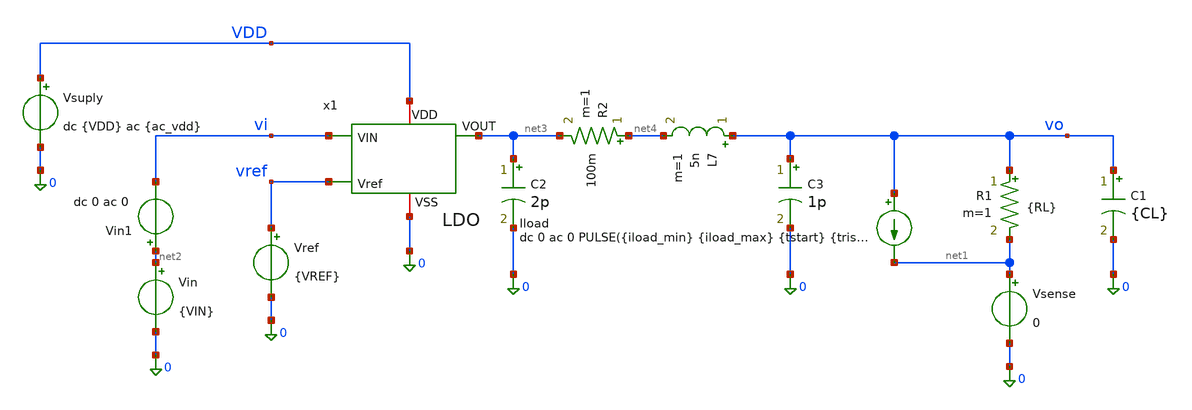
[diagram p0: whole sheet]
** sch_path: xschem/ldo_tb.sch
**.subckt ldo_tb
Vsuply VDD 0 dc {VDD} ac {ac_vdd}
Vref vref 0 {VREF}
Vin net2 0 {VIN}
R1 vo net1 {RL} m=1
C1 vo 0 {CL} m=1
Iload vo net1 dc 0 ac 0 PULSE({iload_min} {iload_max} {tstart} {trise} {tfall} {twidth} {tperiod})
Vsense net1 0 0
Vin1 net2 vi dc 0 ac 0
x1 vi net3 VDD vref 0 LDO
C2 net3 0 2p m=1
R2 net4 net3 100m m=1
L7 vo net4 5n m=1
C3 vo 0 1p m=1
**** begin user architecture code









.lib /foss/pdks/sky130A/libs.tech/ngspice/sky130.lib.spice fs_ll
.option temp=-40
.param VDD = 1.62

.option num_threads=8

.param rsh_var = agauss(0, 0.005, 1)


* Forzar un punto de partida para ayudar a la convergencia
.nodeset V(VO)=1.2
.nodeset V(x1.Vre)=0.6




**parametros_ldo

.param VREF = 0.6
.param VIN = '1*VDD'
.param RL = 240e9
.param CL = 1u
.param tsim = 2m

* Parámetros para la prueba de carga del LDO
.param iload_min = 1u
.param iload_max = 5m
.param tstart   = 30u
.param trise    = 100n
.param tfall    = 100n
.param twidth   = 100u
.param tperiod  = 200u

.param tsim = '3*tperiod'

.param ac_iprobe = 1
.param ac_vdd = 0

.control
let tperiod  = 200u
let tsim = '3*tperiod'


* =========================================================
* 2. AC (Estabilidad) -> Genera plot ac1
* =========================================================
alterparam ac_iprobe = 1
alterparam ac_vdd = 0
reset

ac dec 10 1 1G


let T_loop = v(x1.vre) / v(x1.vre2)
let ldb = vdb(T_loop)
let fase = vp(T_loop) * 180 / pi

write LDO_ac_estability.raw
meas ac ugb WHEN ldb = 0.0
meas ac fase_ugb FIND fase WHEN ldb = 0.0
let margen_fase = fase_ugb
meas ac ganancia_banda_plana find ldb at=1

* =========================================================
* 3. AC (PSRR) -> Genera plot ac2
* =========================================================
alterparam ac_iprobe = 0
alterparam ac_vdd = 1
reset

ac dec 10 10 1G


let psrr1 = v(vdd)/v(vo)
let psrr_db = vdb(psrr1)
write LDO_ac_psrr.raw
meas ac gananciaPSRR_1   find psrr_db at=10
meas ac gananciaPSRR_1k  find psrr_db at=1k
meas ac gananciaPSRR_10k find psrr_db at=10k
meas ac gananciaPSRR_1M  find psrr_db at=1Meg

* =========================================================
* 4. TRANSIENTE (Line Regulation) -> Genera plot tran1
* =========================================================
alterparam ac_iprobe = 0
alterparam ac_vdd = 0
reset

alter @Vin[pwl] = [ 0 1.4 1m 1.8 ]
alter @Iload[pwl] = [ 0 1u 1m 1u ]

tran 1u 1m
write LDO_dc_line.raw

let t_line_ini = 40u
let t_line_fin = 950u

meas tran voline_max MAX v(vo) from=$&t_line_ini to=$&t_line_fin
meas tran voline_min MIN v(vo) from=$&t_line_ini to=$&t_line_fin
let line_regulation_mV = (voline_max - voline_min)*1000
meas tran salida_line avg v(vo) from=$&t_line_ini to=$&t_line_fin
* =========================================================

* 1. TRANSIENTE (Overshoot y Undershoot) -> Genera plot tran2
* =========================================================
alterparam ac_iprobe = 0
alterparam ac_vdd = 0
alterparam RL = 240e9
reset

tran 1u $&tsim
write LDO_tran_picos.raw

let t_ignorar = 150u

meas tran v_estable_ligera FIND v(vo) AT=270u
meas tran v_estable_pesada FIND v(vo) AT=180u
meas tran vo_max MAX v(vo) from=$&t_ignorar to=$&tsim
meas tran vo_min MIN v(vo) from=$&t_ignorar to=$&tsim

let undershoot_mV = (v_estable_ligera - vo_min) * 1e3
let overshoot_mV = (vo_max - v_estable_pesada) * 1e3
meas tran salida_tran avg v(vo) from=$&t_ignorar to=$&tsim


* =========================================================
* 5. TRANSIENTE (Load Regulation) -> Genera plot tran3
* =========================================================
alterparam RL = 240e9
reset
alter @Iload[pwl] = [ 0 1u 1m 5m ]

tran 1u 1m
write LDO_dc_load.raw

meas tran vout_light FIND v(vo) AT=40u
meas tran vout_heavy FIND v(vo) AT=1m
let load_regulation_mV = (vout_light - vout_heavy) * 1000

* =========================================================
* 6. TRANSIENTE (Dropout) -> Genera plot tran4
* =========================================================
alterparam RL = 240
reset
alter @Vin[pwl] = [ 0 2 1m 0 ]
alter @Iload[pwl] = [ 0 1u 1m 1u ]

tran 1u 1m
write LDO_dc_dropout.raw

meas tran vout_nom FIND v(vo) AT=225u
let vout_target = vout_nom * 0.90
meas tran vin_do FIND v(vi) WHEN v(vo) = vout_target fall=1
let dropout_mV = (vin_do - vout_target) * 1e3

* =========================================================
* IMPRESION DE TODOS LOS RESULTADOS CON SETPLOT
* =========================================================

echo '--- RESULTADOS DE TRANSIENTE ---'
setplot tran3
print undershoot_mV overshoot_mV v_estable_ligera v_estable_pesada salida_tran

echo '--- RESULTADOS AC (ESTABILIDAD) ---'
setplot ac1
print ugb fase_ugb margen_fase ganancia_banda_plana

echo '--- RESULTADOS AC (PSRR) ---'
setplot ac2
print gananciaPSRR_1 gananciaPSRR_1k gananciaPSRR_10k gananciaPSRR_1M

echo '--- RESULTADOS REGULACIONES Y DROPOUT ---'
echo '>> Line Regulation'
setplot tran2
print line_regulation_mV salida_line

echo '>> Load Regulation'
setplot tran4
print load_regulation_mV

echo '>> Dropout'
setplot tran5
print dropout_mV vin_do vout_target

.endc






















.control



alterparam RL = 240e9
reset

*  Punto de Operación (.OP)

save all


save @m.x1.xM1.msky130_fd_pr__pfet_01v8_lvt[gm]
save @m.x1.xM1.msky130_fd_pr__pfet_01v8_lvt[gds]
save @m.x1.xM1.msky130_fd_pr__pfet_01v8_lvt[id]
save @m.x1.xM1.msky130_fd_pr__pfet_01v8_lvt[vgs]
save @m.x1.xM1.msky130_fd_pr__pfet_01v8_lvt[vds]
save @m.x1.xM1.msky130_fd_pr__pfet_01v8_lvt[vth]
save @m.x1.xM1.msky130_fd_pr__pfet_01v8_lvt[vdsat]




save @m.x1.x1.xMr.msky130_fd_pr__pfet_01v8_lvt[gm]
save @m.x1.x1.xMr.msky130_fd_pr__pfet_01v8_lvt[gds]
save @m.x1.x1.xMr.msky130_fd_pr__pfet_01v8_lvt[id]
save @m.x1.x1.xMr.msky130_fd_pr__pfet_01v8_lvt[vgs]
save @m.x1.x1.xMr.msky130_fd_pr__pfet_01v8_lvt[vds]
save @m.x1.x1.xMr.msky130_fd_pr__pfet_01v8_lvt[vth]
save @m.x1.x1.xMr.msky130_fd_pr__pfet_01v8_lvt[vdsat]

save @m.x1.x1.xMnref.msky130_fd_pr__nfet_01v8[gm]
save @m.x1.x1.xMnref.msky130_fd_pr__nfet_01v8[gds]
save @m.x1.x1.xMnref.msky130_fd_pr__nfet_01v8[id]
save @m.x1.x1.xMnref.msky130_fd_pr__nfet_01v8[vgs]
save @m.x1.x1.xMnref.msky130_fd_pr__nfet_01v8[vds]
save @m.x1.x1.xMnref.msky130_fd_pr__nfet_01v8[vth]
save @m.x1.x1.xMnref.msky130_fd_pr__nfet_01v8[vdsat]

save @m.x1.xMnl.msky130_fd_pr__nfet_01v8[gm]
save @m.x1.xMnl.msky130_fd_pr__nfet_01v8[gds]
save @m.x1.xMnl.msky130_fd_pr__nfet_01v8[id]
save @m.x1.xMnl.msky130_fd_pr__nfet_01v8[vgs]
save @m.x1.xMnl.msky130_fd_pr__nfet_01v8[vds]
save @m.x1.xMnl.msky130_fd_pr__nfet_01v8[vth]
save @m.x1.xMnl.msky130_fd_pr__nfet_01v8[vdsat]



* --- Etapa Diferencial (Núcleo del OTA) ---

* Mrc1 (pfet_01v8_lvt)
save @m.x1.x1.xMrc1.msky130_fd_pr__pfet_01v8_lvt[gm]
save @m.x1.x1.xMrc1.msky130_fd_pr__pfet_01v8_lvt[gds]
save @m.x1.x1.xMrc1.msky130_fd_pr__pfet_01v8_lvt[id]
save @m.x1.x1.xMrc1.msky130_fd_pr__pfet_01v8_lvt[vgs]
save @m.x1.x1.xMrc1.msky130_fd_pr__pfet_01v8_lvt[vds]
save @m.x1.x1.xMrc1.msky130_fd_pr__pfet_01v8_lvt[vth]
save @m.x1.x1.xMrc1.msky130_fd_pr__pfet_01v8_lvt[vdsat]

* Mn (pfet_01v8)
save @m.x1.x1.xMn.msky130_fd_pr__pfet_01v8_lvt[gm]
save @m.x1.x1.xMn.msky130_fd_pr__pfet_01v8_lvt[gds]
save @m.x1.x1.xMn.msky130_fd_pr__pfet_01v8_lvt[id]
save @m.x1.x1.xMn.msky130_fd_pr__pfet_01v8_lvt[vgs]
save @m.x1.x1.xMn.msky130_fd_pr__pfet_01v8_lvt[vds]
save @m.x1.x1.xMn.msky130_fd_pr__pfet_01v8_lvt[vth]
save @m.x1.x1.xMn.msky130_fd_pr__pfet_01v8_lvt[vdsat]

* Mp (pfet_01v8)
save @m.x1.x1.xMp.msky130_fd_pr__pfet_01v8_lvt[gm]
save @m.x1.x1.xMp.msky130_fd_pr__pfet_01v8_lvt[gds]
save @m.x1.x1.xMp.msky130_fd_pr__pfet_01v8_lvt[id]
save @m.x1.x1.xMp.msky130_fd_pr__pfet_01v8_lvt[vgs]
save @m.x1.x1.xMp.msky130_fd_pr__pfet_01v8_lvt[vds]
save @m.x1.x1.xMp.msky130_fd_pr__pfet_01v8_lvt[vth]
save @m.x1.x1.xMp.msky130_fd_pr__pfet_01v8_lvt[vdsat]

* Mnr (nfet_01v8)
save @m.x1.x1.xMnr.msky130_fd_pr__nfet_01v8[gm]
save @m.x1.x1.xMnr.msky130_fd_pr__nfet_01v8[gds]
save @m.x1.x1.xMnr.msky130_fd_pr__nfet_01v8[id]
save @m.x1.x1.xMnr.msky130_fd_pr__nfet_01v8[vgs]
save @m.x1.x1.xMnr.msky130_fd_pr__nfet_01v8[vds]
save @m.x1.x1.xMnr.msky130_fd_pr__nfet_01v8[vth]
save @m.x1.x1.xMnr.msky130_fd_pr__nfet_01v8[vdsat]

* Mpr (nfet_01v8)
save @m.x1.x1.xMpr.msky130_fd_pr__nfet_01v8[gm]
save @m.x1.x1.xMpr.msky130_fd_pr__nfet_01v8[gds]
save @m.x1.x1.xMpr.msky130_fd_pr__nfet_01v8[id]
save @m.x1.x1.xMpr.msky130_fd_pr__nfet_01v8[vgs]
save @m.x1.x1.xMpr.msky130_fd_pr__nfet_01v8[vds]
save @m.x1.x1.xMpr.msky130_fd_pr__nfet_01v8[vth]
save @m.x1.x1.xMpr.msky130_fd_pr__nfet_01v8[vdsat]


* --- Etapa de Salida ---

* Mrc2 (pfet_01v8_lvt)
save @m.x1.x1.xMrc2.msky130_fd_pr__pfet_01v8_lvt[gm]
save @m.x1.x1.xMrc2.msky130_fd_pr__pfet_01v8_lvt[gds]
save @m.x1.x1.xMrc2.msky130_fd_pr__pfet_01v8_lvt[id]
save @m.x1.x1.xMrc2.msky130_fd_pr__pfet_01v8_lvt[vgs]
save @m.x1.x1.xMrc2.msky130_fd_pr__pfet_01v8_lvt[vds]
save @m.x1.x1.xMrc2.msky130_fd_pr__pfet_01v8_lvt[vth]
save @m.x1.x1.xMrc2.msky130_fd_pr__pfet_01v8_lvt[vdsat]

* Mo (nfet_01v8)
save @m.x1.x1.xMo.msky130_fd_pr__nfet_01v8[gm]
save @m.x1.x1.xMo.msky130_fd_pr__nfet_01v8[gds]
save @m.x1.x1.xMo.msky130_fd_pr__nfet_01v8[id]
save @m.x1.x1.xMo.msky130_fd_pr__nfet_01v8[vgs]
save @m.x1.x1.xMo.msky130_fd_pr__nfet_01v8[vds]
save @m.x1.x1.xMo.msky130_fd_pr__nfet_01v8[vth]
save @m.x1.x1.xMo.msky130_fd_pr__nfet_01v8[vdsat]


op
set filetype=ascii
write LDO_op.raw

















.endc






**** end user architecture code
**.ends

* expanding   symbol:  /foss/designs/LDO-sky130/xschem/LDO.sym # of pins=5
** sym_path: xschem/LDO.sym
** sch_path: xschem/LDO.sch
.subckt LDO VIN VOUT VDD Vref VSS
*.ipin VIN
*.iopin VDD
*.opin VOUT
*.ipin Vref
*.iopin VSS
V1 vre2 Vre 0 ac {ac_iprobe}
x1 VDD Vgp Vref vre2 VSS Vgn_bias OTA
XC1 VOUT Vre sky130_fd_pr__cap_mim_m3_2 W=27 L=25 MF=1 m=1
XM1 VOUT Vgp VIN VDD sky130_fd_pr__pfet_01v8_lvt L=1 W=250 nf=100 ad='int((100 + 1)/2) * 250 / 100 * 0.29'
+ as='int((100 + 2)/2) * 250 / 100 * 0.29' pd='2*int((100 + 1)/2) * (250 / 100 + 0.29)' ps='2*int((100 + 2)/2) * (250 / 100 + 0.29)'
+ nrd='0.29 / 250 ' nrs='0.29 / 250 ' sa=0 sb=0 sd=0 mult=3 m=3
x2 VDD Vgn_bias VSS self_bias
XMnl VOUT Vgn_bias VSS VSS sky130_fd_pr__nfet_01v8 L=0.5 W=20 nf=2 ad='int((2 + 1)/2) * 20 / 2 * 0.29'
+ as='int((2 + 2)/2) * 20 / 2 * 0.29' pd='2*int((2 + 1)/2) * (20 / 2 + 0.29)' ps='2*int((2 + 2)/2) * (20 / 2 + 0.29)'
+ nrd='0.29 / 20 ' nrs='0.29 / 20 ' sa=0 sb=0 sd=0 mult=1 m=1
R8 VOUT Vre {109k*(1+rsh_var)} m=1
R9 Vre VSS {109k*(1+rsh_var)} m=1
.ends


* expanding   symbol:  /foss/designs/LDO-sky130/xschem/OTA.sym # of pins=6
** sym_path: xschem/OTA/OTA.sym
** sch_path: xschem/OTA/OTA.sch
.subckt OTA VDD VO_ota VIN_ota VIP_ota VSS VGN
*.ipin VIN_ota
*.opin VO_ota
*.iopin VSS
*.iopin VDD
*.ipin VIP_ota
*.iopin VGN
XMpr vo1 vd VSS VSS sky130_fd_pr__nfet_01v8 L=1 W=6 nf=4 ad='int((4 + 1)/2) * 6 / 4 * 0.29' as='int((4 + 2)/2) * 6 / 4 * 0.29'
+ pd='2*int((4 + 1)/2) * (6 / 4 + 0.29)' ps='2*int((4 + 2)/2) * (6 / 4 + 0.29)' nrd='0.29 / 6 ' nrs='0.29 / 6 '
+ sa=0 sb=0 sd=0 mult=1 m=1
XMnr vd vd VSS VSS sky130_fd_pr__nfet_01v8 L=1 W=6 nf=4 ad='int((4 + 1)/2) * 6 / 4 * 0.29' as='int((4 + 2)/2) * 6 / 4 * 0.29'
+ pd='2*int((4 + 1)/2) * (6 / 4 + 0.29)' ps='2*int((4 + 2)/2) * (6 / 4 + 0.29)' nrd='0.29 / 6 ' nrs='0.29 / 6 '
+ sa=0 sb=0 sd=0 mult=1 m=1
XMo VO_ota vo1 VSS VSS sky130_fd_pr__nfet_01v8 L=2 W=8 nf=8 ad='int((8 + 1)/2) * 8 / 8 * 0.29' as='int((8 + 2)/2) * 8 / 8 * 0.29'
+ pd='2*int((8 + 1)/2) * (8 / 8 + 0.29)' ps='2*int((8 + 2)/2) * (8 / 8 + 0.29)' nrd='0.29 / 8 ' nrs='0.29 / 8 '
+ sa=0 sb=0 sd=0 mult=1 m=1
XMrc2 VO_ota vgp VDD VDD sky130_fd_pr__pfet_01v8_lvt L=2 W=50 nf=8 ad='int((8 + 1)/2) * 50 / 8 * 0.29'
+ as='int((8 + 2)/2) * 50 / 8 * 0.29' pd='2*int((8 + 1)/2) * (50 / 8 + 0.29)' ps='2*int((8 + 2)/2) * (50 / 8 + 0.29)'
+ nrd='0.29 / 50 ' nrs='0.29 / 50 ' sa=0 sb=0 sd=0 mult=1 m=1
XC1 VO_ota vmiler sky130_fd_pr__cap_mim_m3_2 W=44.6 L=56 MF=1 m=1
XMp vo1 VIP_ota vtail VDD sky130_fd_pr__pfet_01v8_lvt L=1 W=26 nf=4 ad='int((4 + 1)/2) * 26 / 4 * 0.29'
+ as='int((4 + 2)/2) * 26 / 4 * 0.29' pd='2*int((4 + 1)/2) * (26 / 4 + 0.29)' ps='2*int((4 + 2)/2) * (26 / 4 + 0.29)'
+ nrd='0.29 / 26 ' nrs='0.29 / 26 ' sa=0 sb=0 sd=0 mult=1 m=1
XMn vd VIN_ota vtail VDD sky130_fd_pr__pfet_01v8_lvt L=1 W=26 nf=4 ad='int((4 + 1)/2) * 26 / 4 * 0.29'
+ as='int((4 + 2)/2) * 26 / 4 * 0.29' pd='2*int((4 + 1)/2) * (26 / 4 + 0.29)' ps='2*int((4 + 2)/2) * (26 / 4 + 0.29)'
+ nrd='0.29 / 26 ' nrs='0.29 / 26 ' sa=0 sb=0 sd=0 mult=1 m=1
XMrc1 vtail vgp VDD VDD sky130_fd_pr__pfet_01v8_lvt L=1 W=50 nf=8 ad='int((8 + 1)/2) * 50 / 8 * 0.29'
+ as='int((8 + 2)/2) * 50 / 8 * 0.29' pd='2*int((8 + 1)/2) * (50 / 8 + 0.29)' ps='2*int((8 + 2)/2) * (50 / 8 + 0.29)'
+ nrd='0.29 / 50 ' nrs='0.29 / 50 ' sa=0 sb=0 sd=0 mult=1 m=1
XMr vgp vgp VDD VDD sky130_fd_pr__pfet_01v8_lvt L=1 W=12.5 nf=2 ad='int((2 + 1)/2) * 12.5 / 2 * 0.29'
+ as='int((2 + 2)/2) * 12.5 / 2 * 0.29' pd='2*int((2 + 1)/2) * (12.5 / 2 + 0.29)' ps='2*int((2 + 2)/2) * (12.5 / 2 + 0.29)'
+ nrd='0.29 / 12.5 ' nrs='0.29 / 12.5 ' sa=0 sb=0 sd=0 mult=1 m=1
XMnref vgp VGN VSS VSS sky130_fd_pr__nfet_01v8 L=1 W=8 nf=1 ad='int((1 + 1)/2) * 8 / 1 * 0.29' as='int((1 + 2)/2) * 8 / 1 * 0.29'
+ pd='2*int((1 + 1)/2) * (8 / 1 + 0.29)' ps='2*int((1 + 2)/2) * (8 / 1 + 0.29)' nrd='0.29 / 8 ' nrs='0.29 / 8 '
+ sa=0 sb=0 sd=0 mult=1 m=1
XR10 vo1 vmiler VSS sky130_fd_pr__res_xhigh_po_0p35 L=90.72 mult=1 m=1
.ends


* expanding   symbol:  /foss/designs/OSCAR/xschem/Iref/self_bias.sym # of pins=3
** sym_path: xschem/Iref/self_bias.sym
** sch_path: xschem/Iref/self_bias.sch
.subckt self_bias VDD VR VSS
*.iopin VR
*.iopin VDD
*.iopin VSS
XMp4 vgp_self vgp_self VDD VDD sky130_fd_pr__pfet_01v8_lvt L=1 W=30 nf=6 ad='int((6 + 1)/2) * 30 / 6 * 0.29'
+ as='int((6 + 2)/2) * 30 / 6 * 0.29' pd='2*int((6 + 1)/2) * (30 / 6 + 0.29)' ps='2*int((6 + 2)/2) * (30 / 6 + 0.29)'
+ nrd='0.29 / 30 ' nrs='0.29 / 30 ' sa=0 sb=0 sd=0 mult=1 m=1
XMp3 VDI vgp_self VDD VDD sky130_fd_pr__pfet_01v8_lvt L=1 W=30 nf=6 ad='int((6 + 1)/2) * 30 / 6 * 0.29'
+ as='int((6 + 2)/2) * 30 / 6 * 0.29' pd='2*int((6 + 1)/2) * (30 / 6 + 0.29)' ps='2*int((6 + 2)/2) * (30 / 6 + 0.29)'
+ nrd='0.29 / 30 ' nrs='0.29 / 30 ' sa=0 sb=0 sd=0 mult=1 m=1
XMs2 VDinv VR vp1 VDD sky130_fd_pr__pfet_01v8_lvt L=5 W=0.5 nf=1 ad='int((1 + 1)/2) * 0.5 / 1 * 0.29'
+ as='int((1 + 2)/2) * 0.5 / 1 * 0.29' pd='2*int((1 + 1)/2) * (0.5 / 1 + 0.29)' ps='2*int((1 + 2)/2) * (0.5 / 1 + 0.29)'
+ nrd='0.29 / 0.5 ' nrs='0.29 / 0.5 ' sa=0 sb=0 sd=0 mult=1 m=1
XMn2 vgp_self VDI VR VSS sky130_fd_pr__nfet_01v8 L=1 W=24 nf=6 ad='int((6 + 1)/2) * 24 / 6 * 0.29' as='int((6 + 2)/2) * 24 / 6 * 0.29'
+ pd='2*int((6 + 1)/2) * (24 / 6 + 0.29)' ps='2*int((6 + 2)/2) * (24 / 6 + 0.29)' nrd='0.29 / 24 ' nrs='0.29 / 24 '
+ sa=0 sb=0 sd=0 mult=1 m=1
XMn1 VDI VR VSS VSS sky130_fd_pr__nfet_01v8 L=1 W=5 nf=5 ad='int((5 + 1)/2) * 5 / 5 * 0.29' as='int((5 + 2)/2) * 5 / 5 * 0.29'
+ pd='2*int((5 + 1)/2) * (5 / 5 + 0.29)' ps='2*int((5 + 2)/2) * (5 / 5 + 0.29)' nrd='0.29 / 5 ' nrs='0.29 / 5 '
+ sa=0 sb=0 sd=0 mult=1 m=1
XMs3 VDinv VR VSS VSS sky130_fd_pr__nfet_01v8 L=1 W=20 nf=5 ad='int((5 + 1)/2) * 20 / 5 * 0.29' as='int((5 + 2)/2) * 20 / 5 * 0.29'
+ pd='2*int((5 + 1)/2) * (20 / 5 + 0.29)' ps='2*int((5 + 2)/2) * (20 / 5 + 0.29)' nrd='0.29 / 20 ' nrs='0.29 / 20 '
+ sa=0 sb=0 sd=0 mult=1 m=1
XMs1 vgp_self VDinv VSS VSS sky130_fd_pr__nfet_01v8 L=1 W=2 nf=2 ad='int((2 + 1)/2) * 2 / 2 * 0.29' as='int((2 + 2)/2) * 2 / 2 * 0.29'
+ pd='2*int((2 + 1)/2) * (2 / 2 + 0.29)' ps='2*int((2 + 2)/2) * (2 / 2 + 0.29)' nrd='0.29 / 2 ' nrs='0.29 / 2 '
+ sa=0 sb=0 sd=0 mult=1 m=1
XR11 VSS VR VSS sky130_fd_pr__res_xhigh_po_0p69 L=20.7 mult=1 m=1
XMs4 vp1 VR vp2 VDD sky130_fd_pr__pfet_01v8_lvt L=5 W=0.5 nf=1 ad='int((1 + 1)/2) * 0.5 / 1 * 0.29' as='int((1 + 2)/2) * 0.5 / 1 * 0.29'
+ pd='2*int((1 + 1)/2) * (0.5 / 1 + 0.29)' ps='2*int((1 + 2)/2) * (0.5 / 1 + 0.29)' nrd='0.29 / 0.5 ' nrs='0.29 / 0.5 '
+ sa=0 sb=0 sd=0 mult=1 m=1
XMs5 vp2 VR vp3 VDD sky130_fd_pr__pfet_01v8_lvt L=5 W=0.5 nf=1 ad='int((1 + 1)/2) * 0.5 / 1 * 0.29' as='int((1 + 2)/2) * 0.5 / 1 * 0.29'
+ pd='2*int((1 + 1)/2) * (0.5 / 1 + 0.29)' ps='2*int((1 + 2)/2) * (0.5 / 1 + 0.29)' nrd='0.29 / 0.5 ' nrs='0.29 / 0.5 '
+ sa=0 sb=0 sd=0 mult=1 m=1
XMs6 vp3 VR vp4 VDD sky130_fd_pr__pfet_01v8_lvt L=5 W=0.5 nf=1 ad='int((1 + 1)/2) * 0.5 / 1 * 0.29' as='int((1 + 2)/2) * 0.5 / 1 * 0.29'
+ pd='2*int((1 + 1)/2) * (0.5 / 1 + 0.29)' ps='2*int((1 + 2)/2) * (0.5 / 1 + 0.29)' nrd='0.29 / 0.5 ' nrs='0.29 / 0.5 '
+ sa=0 sb=0 sd=0 mult=1 m=1
XMs7 vp4 VR VDD VDD sky130_fd_pr__pfet_01v8_lvt L=5 W=0.5 nf=1 ad='int((1 + 1)/2) * 0.5 / 1 * 0.29' as='int((1 + 2)/2) * 0.5 / 1 * 0.29'
+ pd='2*int((1 + 1)/2) * (0.5 / 1 + 0.29)' ps='2*int((1 + 2)/2) * (0.5 / 1 + 0.29)' nrd='0.29 / 0.5 ' nrs='0.29 / 0.5 '
+ sa=0 sb=0 sd=0 mult=1 m=1
.ends

.end
